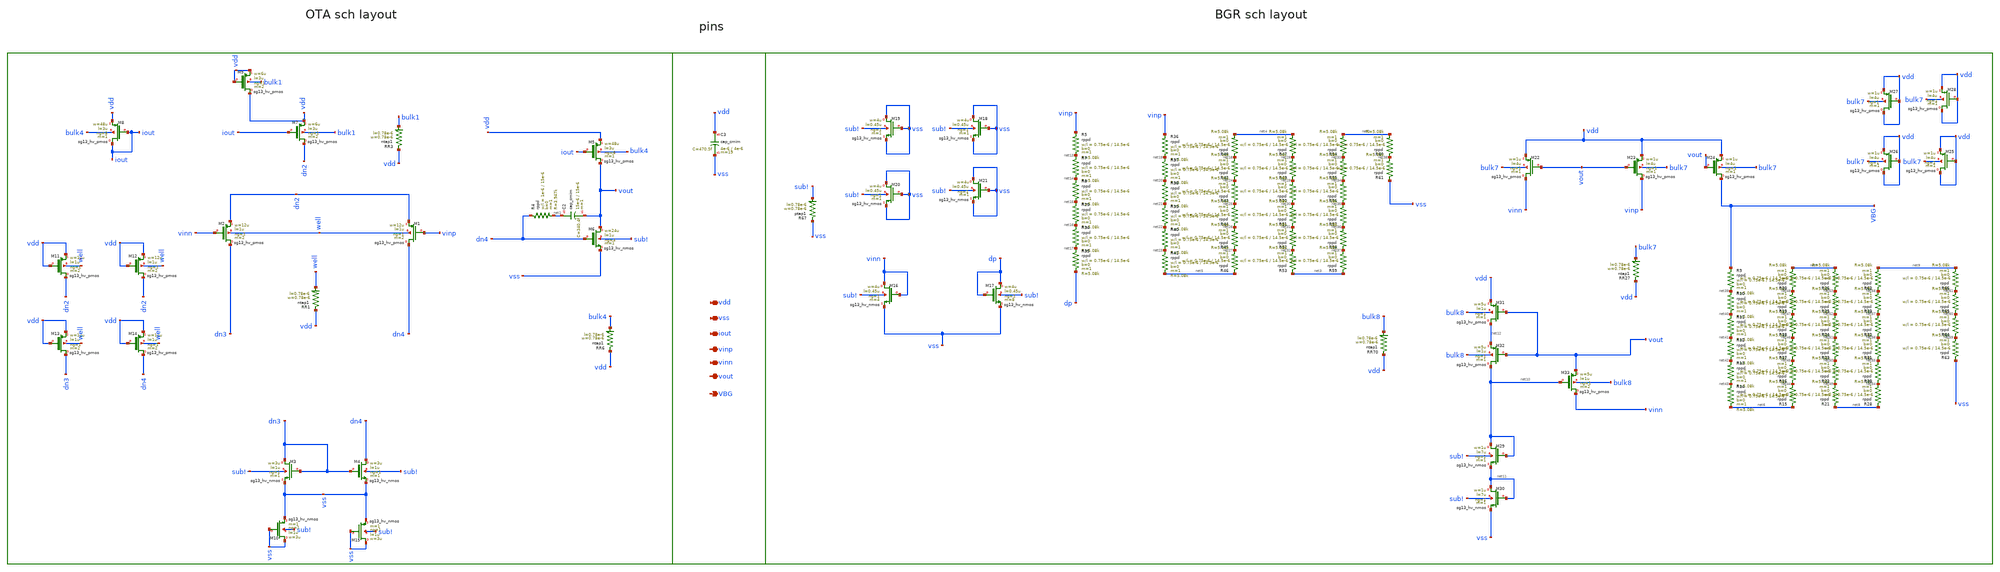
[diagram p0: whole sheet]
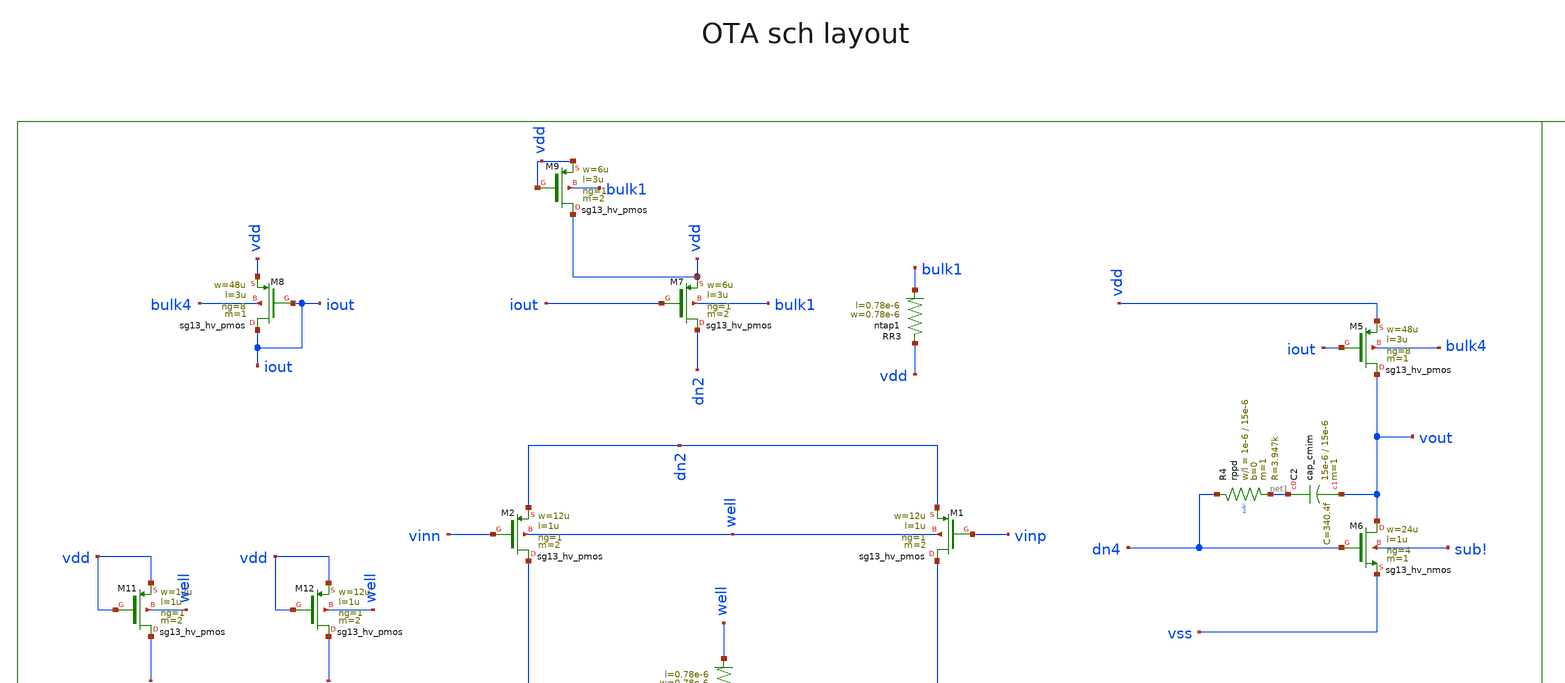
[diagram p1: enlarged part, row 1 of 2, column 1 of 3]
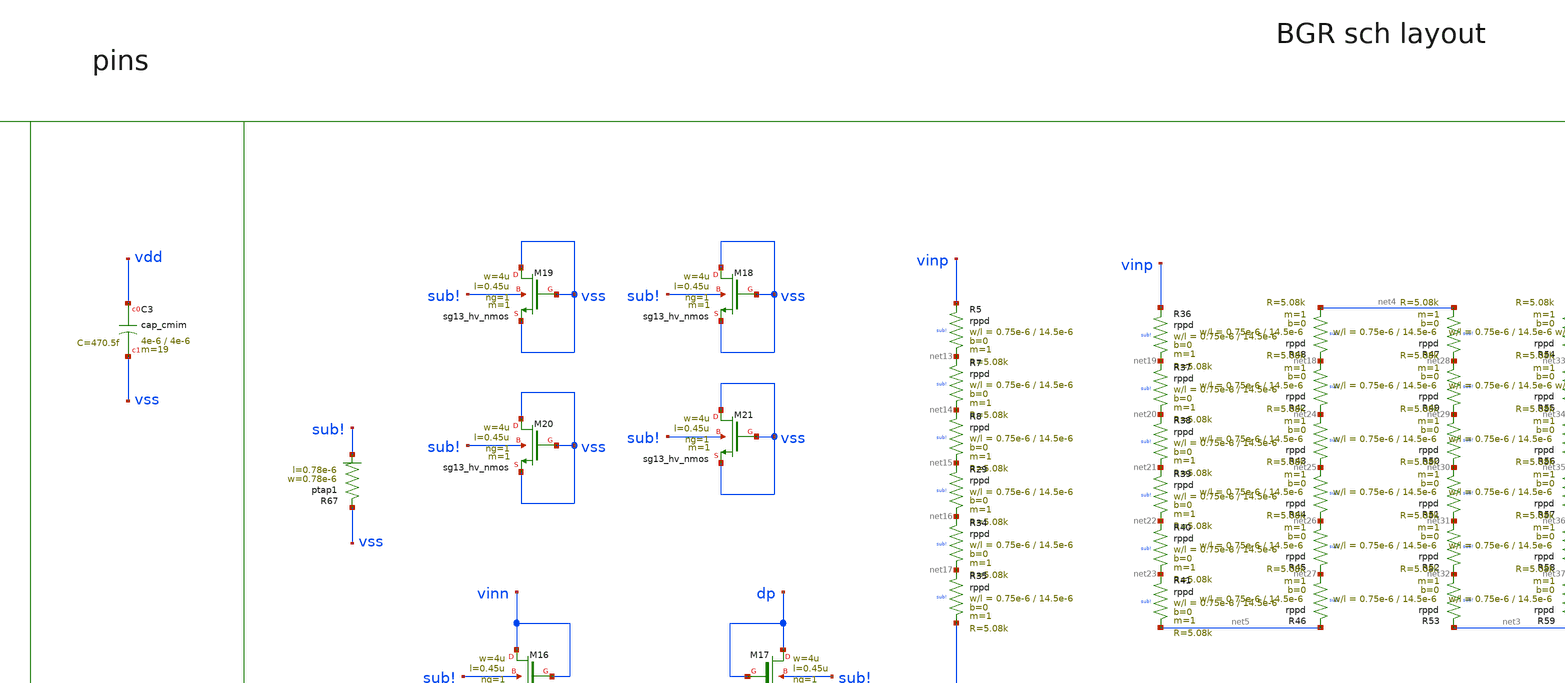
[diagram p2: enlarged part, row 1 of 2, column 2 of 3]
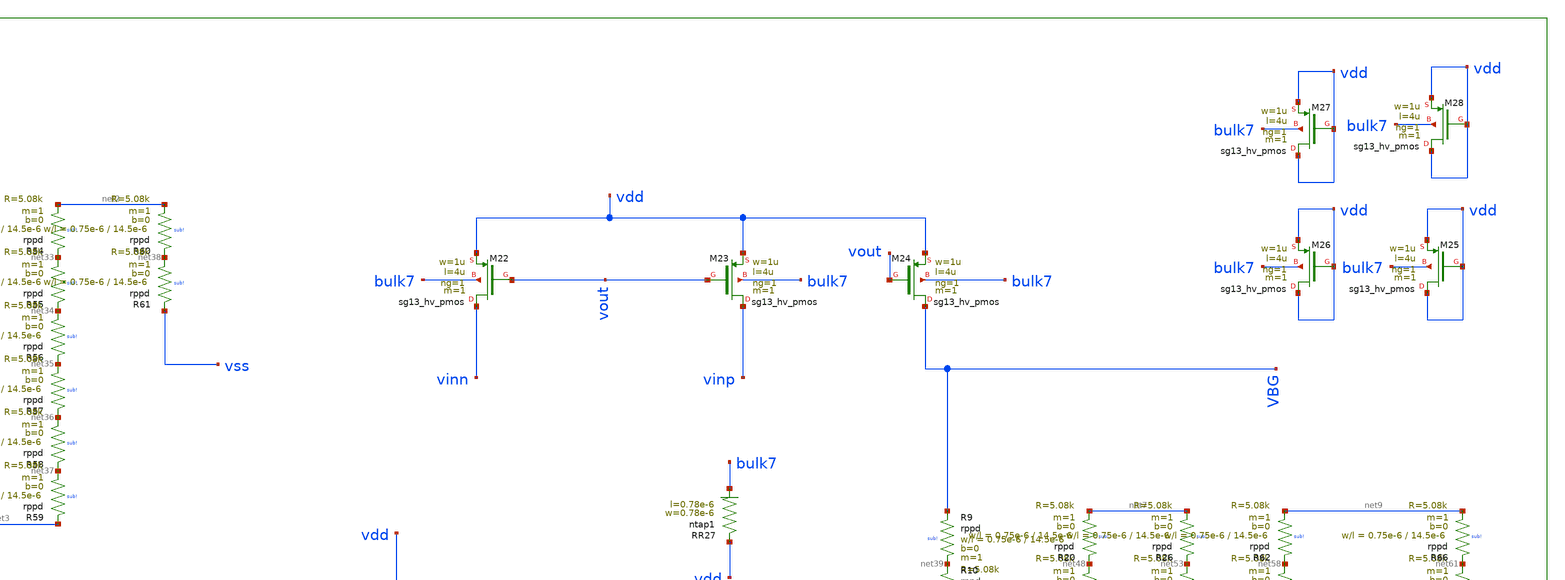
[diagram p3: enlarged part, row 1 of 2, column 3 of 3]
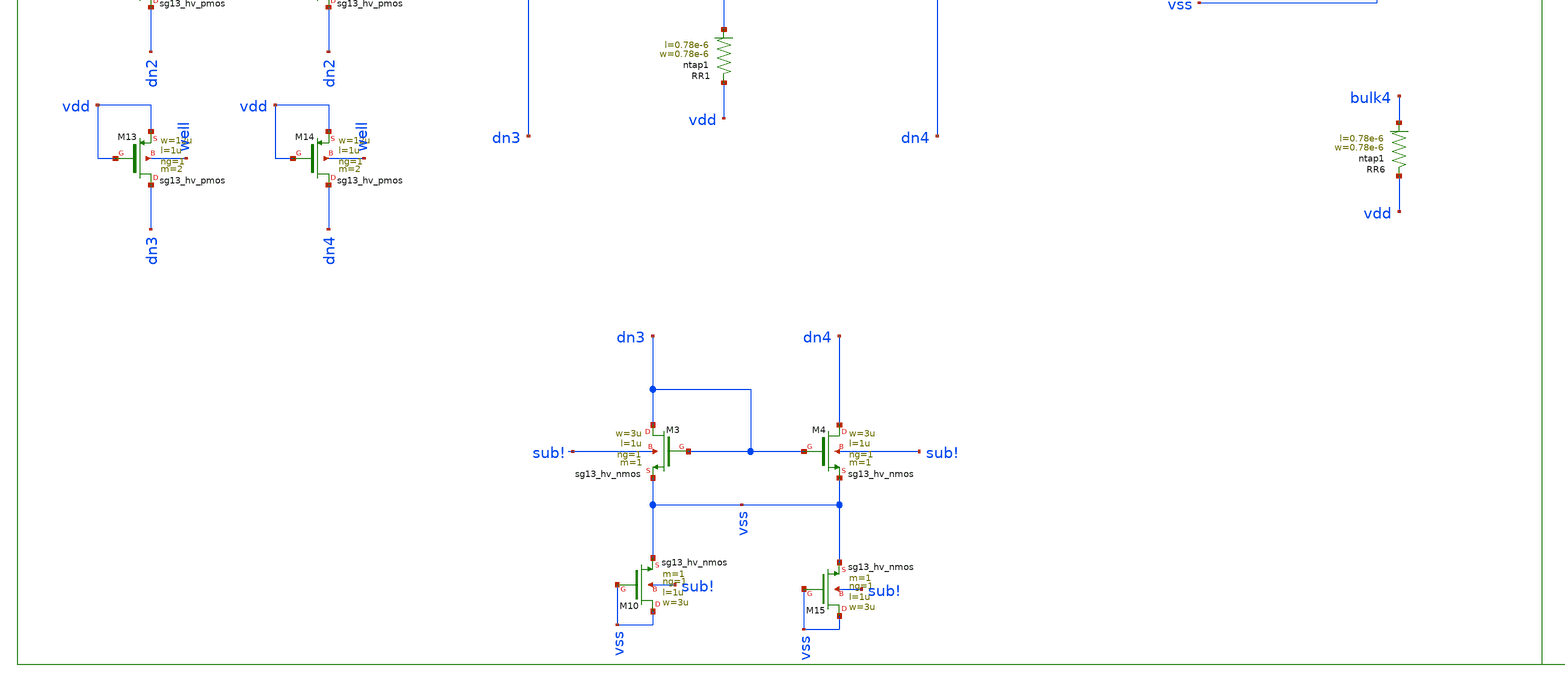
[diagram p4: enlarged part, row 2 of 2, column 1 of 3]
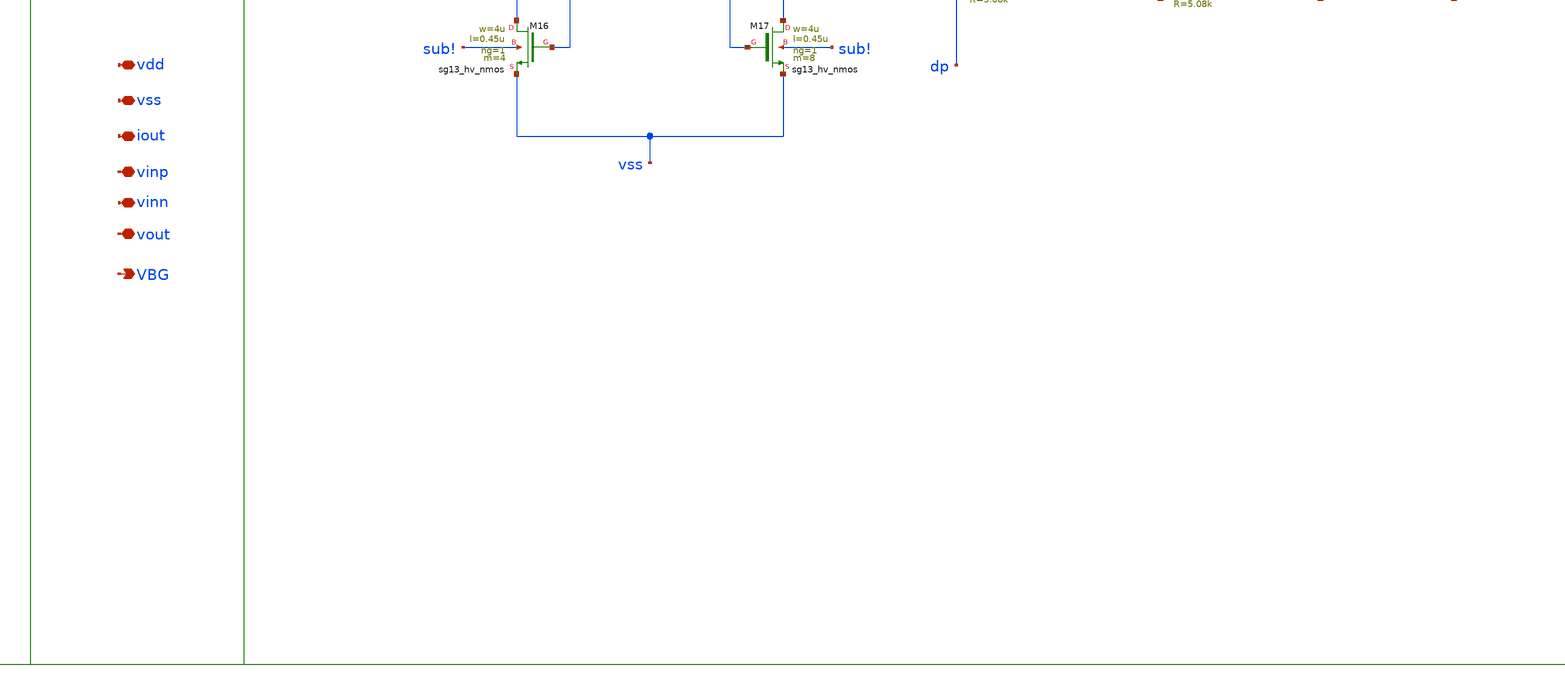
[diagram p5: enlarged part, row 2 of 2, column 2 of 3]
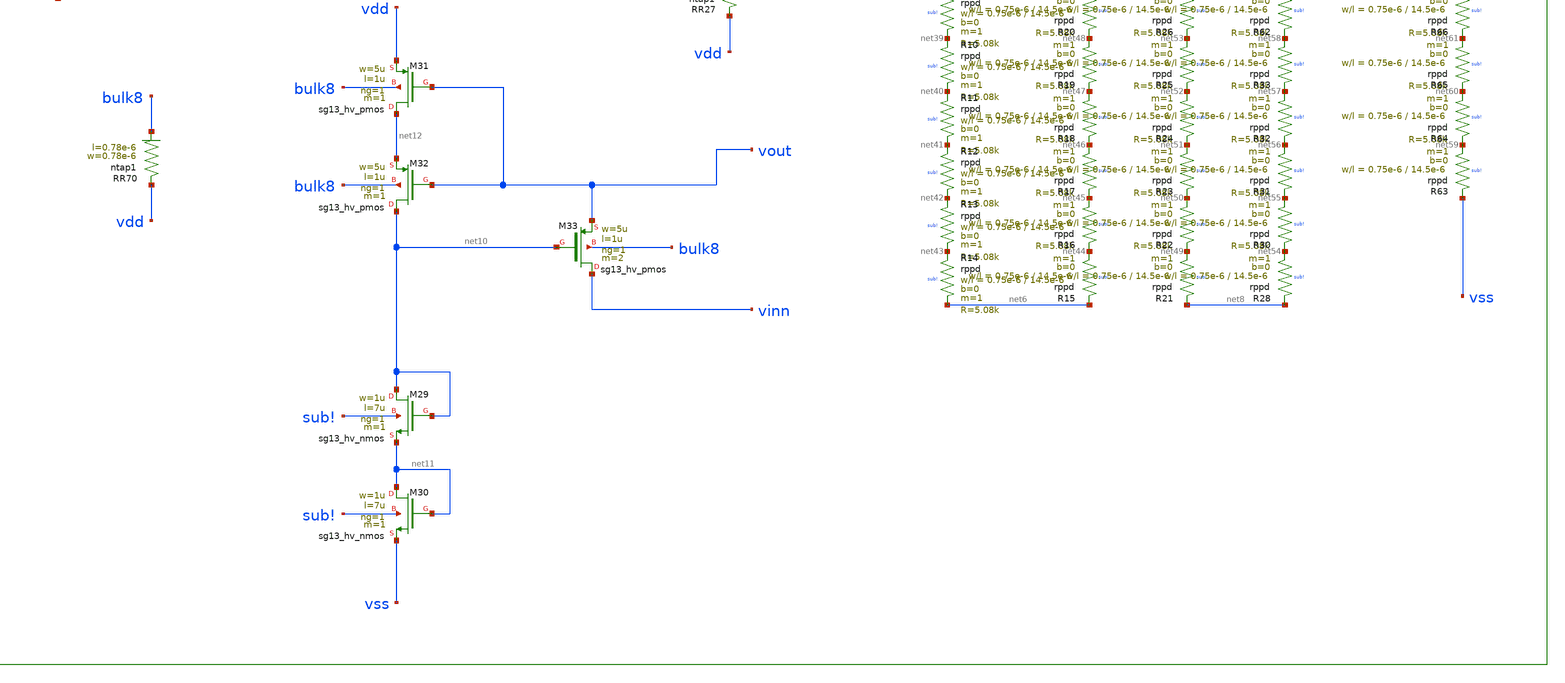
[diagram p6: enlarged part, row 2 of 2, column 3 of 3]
** sch_path: dependencies/pmu_ip/dependencies/bgr_ip/bgr_ip-main/schematic/xschem/bgr_ip.sch
**.subckt bgr_ip vdd vss iout vinp vinn vout VBG
*.iopin vdd
*.iopin vss
*.iopin iout
*.iopin vinp
*.iopin vinn
*.iopin vout
*.opin VBG
XM1 dn4 vinp dn2 well sg13_hv_pmos w=12u l=1u ng=1 m=2 mm_ok=1
XM2 dn3 vinn dn2 well sg13_hv_pmos w=12u l=1u ng=1 m=2 mm_ok=1
XM11 dn2 vdd vdd well sg13_hv_pmos w=12u l=1u ng=1 m=2 mm_ok=1
XM12 dn2 vdd vdd well sg13_hv_pmos w=12u l=1u ng=1 m=2 mm_ok=1
XM13 dn3 vdd vdd well sg13_hv_pmos w=12u l=1u ng=1 m=2 mm_ok=1
XM14 dn4 vdd vdd well sg13_hv_pmos w=12u l=1u ng=1 m=2 mm_ok=1
XR1 vdd well ntap1 R=262.8 w=0.78e-6 l=0.78e-6
XR3 vdd bulk1 ntap1 R=262.8 w=0.78e-6 l=0.78e-6
XC2 net1 vout cap_cmim w=15e-6 l=15e-6 m=1 mm_ok=1
XR4 dn4 net1 sub! rppd w=1e-6 l=15e-6 m=1 b=0 mm_ok=1
XR6 vdd bulk4 ntap1 R=262.8 w=0.78e-6 l=0.78e-6
XM5 vout iout vdd bulk4 sg13_hv_pmos w=48u l=3u ng=8 m=1 mm_ok=1
XM6 vout dn4 vss sub! sg13_hv_nmos w=24u l=1u ng=4 m=1 mm_ok=1
XM7 dn2 iout vdd bulk1 sg13_hv_pmos w=6u l=3u ng=1 m=2 mm_ok=1
XM8 iout iout vdd bulk4 sg13_hv_pmos w=48u l=3u ng=8 m=1 mm_ok=1
XM3 dn3 dn3 vss sub! sg13_hv_nmos w=3u l=1u ng=1 m=1 mm_ok=1
XM4 dn4 dn3 vss sub! sg13_hv_nmos w=3u l=1u ng=1 m=1 mm_ok=1
XM9 vdd vdd vdd bulk1 sg13_hv_pmos w=6u l=3u ng=1 m=2 mm_ok=1
XM10 vss vss vss sub! sg13_hv_nmos w=3u l=1u ng=1 m=1 mm_ok=1
XM15 vss vss vss sub! sg13_hv_nmos w=3u l=1u ng=1 m=1 mm_ok=1
XM16 vinn vinn vss sub! sg13_hv_nmos w=4u l=0.45u ng=1 m=4 mm_ok=1
XM17 dp dp vss sub! sg13_hv_nmos w=4u l=0.45u ng=1 m=8 mm_ok=1
XM18 vss vss vss sub! sg13_hv_nmos w=4u l=0.45u ng=1 m=1 mm_ok=1
XM19 vss vss vss sub! sg13_hv_nmos w=4u l=0.45u ng=1 m=1 mm_ok=1
XM20 vss vss vss sub! sg13_hv_nmos w=4u l=0.45u ng=1 m=1 mm_ok=1
XM21 vss vss vss sub! sg13_hv_nmos w=4u l=0.45u ng=1 m=1 mm_ok=1
XR67 vss sub! ptap1 R=262.8 w=0.78e-6 l=0.78e-6
XR5 vinp net13 sub! rppd w=0.75e-6 l=14.5e-6 m=1 b=0 mm_ok=1
XR7 net13 net14 sub! rppd w=0.75e-6 l=14.5e-6 m=1 b=0 mm_ok=1
XR8 net14 net15 sub! rppd w=0.75e-6 l=14.5e-6 m=1 b=0 mm_ok=1
XR29 net15 net16 sub! rppd w=0.75e-6 l=14.5e-6 m=1 b=0 mm_ok=1
XR34 net16 net17 sub! rppd w=0.75e-6 l=14.5e-6 m=1 b=0 mm_ok=1
XR35 net17 dp sub! rppd w=0.75e-6 l=14.5e-6 m=1 b=0 mm_ok=1
XR48 net18 net4 sub! rppd w=0.75e-6 l=14.5e-6 m=1 b=0 mm_ok=1
XR36 vinp net19 sub! rppd w=0.75e-6 l=14.5e-6 m=1 b=0 mm_ok=1
XR37 net19 net20 sub! rppd w=0.75e-6 l=14.5e-6 m=1 b=0 mm_ok=1
XR38 net20 net21 sub! rppd w=0.75e-6 l=14.5e-6 m=1 b=0 mm_ok=1
XR39 net21 net22 sub! rppd w=0.75e-6 l=14.5e-6 m=1 b=0 mm_ok=1
XR40 net22 net23 sub! rppd w=0.75e-6 l=14.5e-6 m=1 b=0 mm_ok=1
XR41 net23 net5 sub! rppd w=0.75e-6 l=14.5e-6 m=1 b=0 mm_ok=1
XR42 net24 net18 sub! rppd w=0.75e-6 l=14.5e-6 m=1 b=0 mm_ok=1
XR43 net25 net24 sub! rppd w=0.75e-6 l=14.5e-6 m=1 b=0 mm_ok=1
XR44 net26 net25 sub! rppd w=0.75e-6 l=14.5e-6 m=1 b=0 mm_ok=1
XR45 net27 net26 sub! rppd w=0.75e-6 l=14.5e-6 m=1 b=0 mm_ok=1
XR46 net5 net27 sub! rppd w=0.75e-6 l=14.5e-6 m=1 b=0 mm_ok=1
XR47 net28 net4 sub! rppd w=0.75e-6 l=14.5e-6 m=1 b=0 mm_ok=1
XR49 net29 net28 sub! rppd w=0.75e-6 l=14.5e-6 m=1 b=0 mm_ok=1
XR50 net30 net29 sub! rppd w=0.75e-6 l=14.5e-6 m=1 b=0 mm_ok=1
XR51 net31 net30 sub! rppd w=0.75e-6 l=14.5e-6 m=1 b=0 mm_ok=1
XR52 net32 net31 sub! rppd w=0.75e-6 l=14.5e-6 m=1 b=0 mm_ok=1
XR53 net3 net32 sub! rppd w=0.75e-6 l=14.5e-6 m=1 b=0 mm_ok=1
XR54 net33 net2 sub! rppd w=0.75e-6 l=14.5e-6 m=1 b=0 mm_ok=1
XR55 net34 net33 sub! rppd w=0.75e-6 l=14.5e-6 m=1 b=0 mm_ok=1
XR56 net35 net34 sub! rppd w=0.75e-6 l=14.5e-6 m=1 b=0 mm_ok=1
XR57 net36 net35 sub! rppd w=0.75e-6 l=14.5e-6 m=1 b=0 mm_ok=1
XR58 net37 net36 sub! rppd w=0.75e-6 l=14.5e-6 m=1 b=0 mm_ok=1
XR59 net3 net37 sub! rppd w=0.75e-6 l=14.5e-6 m=1 b=0 mm_ok=1
XR60 net38 net2 sub! rppd w=0.75e-6 l=14.5e-6 m=1 b=0 mm_ok=1
XR61 vss net38 sub! rppd w=0.75e-6 l=14.5e-6 m=1 b=0 mm_ok=1
XM22 vinn vout vdd bulk7 sg13_hv_pmos w=1u l=4u ng=1 m=1 mm_ok=1
XM23 vinp vout vdd bulk7 sg13_hv_pmos w=1u l=4u ng=1 m=1 mm_ok=1
XM24 VBG vout vdd bulk7 sg13_hv_pmos w=1u l=4u ng=1 m=1 mm_ok=1
XR27 vdd bulk7 ntap1 R=262.8 w=0.78e-6 l=0.78e-6
XR9 VBG net39 sub! rppd w=0.75e-6 l=14.5e-6 m=1 b=0 mm_ok=1
XR10 net39 net40 sub! rppd w=0.75e-6 l=14.5e-6 m=1 b=0 mm_ok=1
XR11 net40 net41 sub! rppd w=0.75e-6 l=14.5e-6 m=1 b=0 mm_ok=1
XR12 net41 net42 sub! rppd w=0.75e-6 l=14.5e-6 m=1 b=0 mm_ok=1
XR13 net42 net43 sub! rppd w=0.75e-6 l=14.5e-6 m=1 b=0 mm_ok=1
XR14 net43 net6 sub! rppd w=0.75e-6 l=14.5e-6 m=1 b=0 mm_ok=1
XR15 net6 net44 sub! rppd w=0.75e-6 l=14.5e-6 m=1 b=0 mm_ok=1
XR16 net44 net45 sub! rppd w=0.75e-6 l=14.5e-6 m=1 b=0 mm_ok=1
XR17 net45 net46 sub! rppd w=0.75e-6 l=14.5e-6 m=1 b=0 mm_ok=1
XR18 net46 net47 sub! rppd w=0.75e-6 l=14.5e-6 m=1 b=0 mm_ok=1
XR19 net47 net48 sub! rppd w=0.75e-6 l=14.5e-6 m=1 b=0 mm_ok=1
XR20 net48 net7 sub! rppd w=0.75e-6 l=14.5e-6 m=1 b=0 mm_ok=1
XR21 net8 net49 sub! rppd w=0.75e-6 l=14.5e-6 m=1 b=0 mm_ok=1
XR22 net49 net50 sub! rppd w=0.75e-6 l=14.5e-6 m=1 b=0 mm_ok=1
XR23 net50 net51 sub! rppd w=0.75e-6 l=14.5e-6 m=1 b=0 mm_ok=1
XR24 net51 net52 sub! rppd w=0.75e-6 l=14.5e-6 m=1 b=0 mm_ok=1
XR25 net52 net53 sub! rppd w=0.75e-6 l=14.5e-6 m=1 b=0 mm_ok=1
XR26 net53 net7 sub! rppd w=0.75e-6 l=14.5e-6 m=1 b=0 mm_ok=1
XR28 net8 net54 sub! rppd w=0.75e-6 l=14.5e-6 m=1 b=0 mm_ok=1
XR30 net54 net55 sub! rppd w=0.75e-6 l=14.5e-6 m=1 b=0 mm_ok=1
XR31 net55 net56 sub! rppd w=0.75e-6 l=14.5e-6 m=1 b=0 mm_ok=1
XR32 net56 net57 sub! rppd w=0.75e-6 l=14.5e-6 m=1 b=0 mm_ok=1
XR33 net57 net58 sub! rppd w=0.75e-6 l=14.5e-6 m=1 b=0 mm_ok=1
XR62 net58 net9 sub! rppd w=0.75e-6 l=14.5e-6 m=1 b=0 mm_ok=1
XR63 vss net59 sub! rppd w=0.75e-6 l=14.5e-6 m=1 b=0 mm_ok=1
XR64 net59 net60 sub! rppd w=0.75e-6 l=14.5e-6 m=1 b=0 mm_ok=1
XR65 net60 net61 sub! rppd w=0.75e-6 l=14.5e-6 m=1 b=0 mm_ok=1
XR66 net61 net9 sub! rppd w=0.75e-6 l=14.5e-6 m=1 b=0 mm_ok=1
XM25 vdd vdd vdd bulk7 sg13_hv_pmos w=1u l=4u ng=1 m=1 mm_ok=1
XM26 vdd vdd vdd bulk7 sg13_hv_pmos w=1u l=4u ng=1 m=1 mm_ok=1
XM27 vdd vdd vdd bulk7 sg13_hv_pmos w=1u l=4u ng=1 m=1 mm_ok=1
XM28 vdd vdd vdd bulk7 sg13_hv_pmos w=1u l=4u ng=1 m=1 mm_ok=1
XM29 net10 net10 net11 sub! sg13_hv_nmos w=1u l=7u ng=1 m=1 mm_ok=1
XM30 net11 net11 vss sub! sg13_hv_nmos w=1u l=7u ng=1 m=1 mm_ok=1
XM31 net12 vout vdd bulk8 sg13_hv_pmos w=5u l=1u ng=1 m=1 mm_ok=1
XM32 net10 vout net12 bulk8 sg13_hv_pmos w=5u l=1u ng=1 m=1 mm_ok=1
XM33 vinn net10 vout bulk8 sg13_hv_pmos w=5u l=1u ng=1 m=2 mm_ok=1
XR70 vdd bulk8 ntap1 R=262.8 w=0.78e-6 l=0.78e-6
XC3 vdd vss cap_cmim w=4e-6 l=4e-6 m=19 mm_ok=1
**.ends
.end
